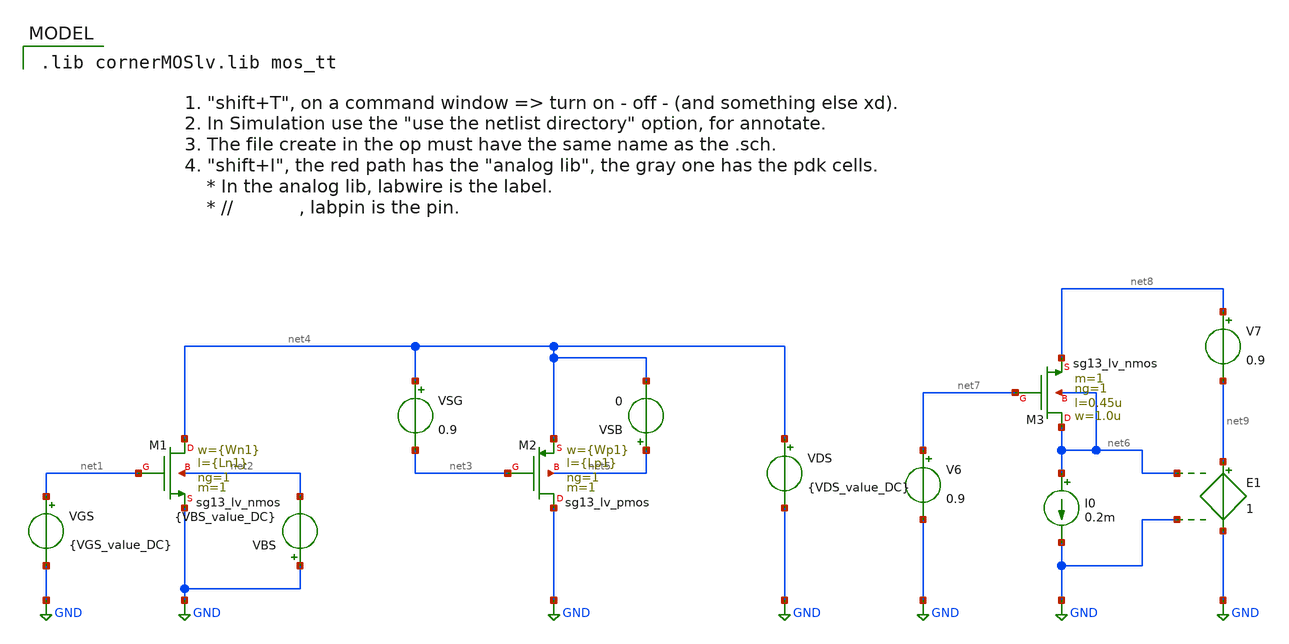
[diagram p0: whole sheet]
** sch_path: ADC8711-main/testbenches/tran/xschem/CMOSCHART_sg130_lv_tb.sch
**.subckt CMOSCHART_sg130_lv_tb
VGS net1 GND {VGS_value_DC}
VDS net4 GND {VDS_value_DC}
VBS GND net2 {VBS_value_DC}
VSG net4 net3 0.9
VSB net5 net4 0
I0 net6 GND 0.2m
V6 net7 GND 0.9
V7 net8 net9 0.9
E1 net9 GND net6 GND 1
XM1 net4 net1 GND net2 sg13_lv_nmos w={Wn1} l={Ln1} ng=1 m=1 mm_ok=1
XM2 GND net3 net4 net5 sg13_lv_pmos w={Wp1} l={Lp1} ng=1 m=1 mm_ok=1
XM3 net6 net7 net8 net6 sg13_lv_nmos w=1.0u l=0.45u ng=1 m=1 mm_ok=1
**** begin user architecture code



.op
.save all
.control

run
let Vgsn = @n.xm1.nsg13_lv_nmos[vgs]
let Vdsn = @n.xm1.nsg13_lv_nmos[vds]
let idn = @n.xm1.nsg13_lv_nmos[ids]
let gmn = @n.xm1.nsg13_lv_nmos[gm]
let vdsatn = @n.xm1.nsg13_lv_nmos[vsat]
let vthn = @n.xm1.nsg13_lv_nmos[vth]
let ron = @n.xm1.nsg13_lv_nmos[gds]
let cggn = @n.xm1.nsg13_lv_nmos[cgg]
let gm_idn = gmn/idn
let ftn = gmn / (6.283 * cggn)
let ftgm_idn = ftn * (gmn/idn)
let aon = gmn*ron
let Vovn = Vgsn - vthn
let deltaVdsn = Vdsn - vdsatn

print Vgsn Vdsn idn vdsatn vthn deltaVdsn Vovn gmn ron cggn gm_idn ftn ftgm_idn aon

write CMOSCHART_sg130_lv_tb.raw
set appendwrite


.endc





.save @n.xm1.nsg13_lv_nmos[ids]
.save @n.xm1.nsg13_lv_nmos[gm]
.save @n.xm1.nsg13_lv_nmos[vds]
.save @n.xm1.nsg13_lv_nmos[vsat]
.save @n.xm1.nsg13_lv_nmos[cgg]
.save @n.xm1.nsg13_lv_nmos[gds]


.dc VGS 0.0 1.8 0.01
.control
run

let idn = @n.xm1.nsg13_lv_nmos[ids]
let gmn = @n.xm1.nsg13_lv_nmos[gm]
let vdsatn = @n.xm1.nsg13_lv_nmos[vsat]
let gm_idn = gmn/idn
let cggn = @n.xm1.nsg13_lv_nmos[cgg]
let ftn = gmn/(6.283*cggn)
let ftgmidn = ftn*gm_idn
let ron = 1/@n.xm1.nsg13_lv_nmos[gds]
let aon = gmn*ron
let vds = @n.xm1.nsg13_lv_nmos[vds]
print vds

*use if you want to design with the gmoverid curve
meas dc VGS_meas WHEN gm_idn=13.57
*measure parameters of interest
meas dc aon_meas FIND aon WHEN v-sweep=VGS_meas
meas dc ftn_meas FIND ftn WHEN v-sweep=VGS_meas
meas dc idn_meas FIND idn WHEN v-sweep=VGS_meas
meas dc gmn_meas FIND gmn WHEN v-sweep=VGS_meas
meas dc gm_idn_meas FIND gm_idn WHEN v-sweep=VGS_meas

*use if you want to design with the vdsat curve
* To obtain the xvalue
*meas dc VGS_meas WHEN vdsatn=200m
* To obtain the yvalue
*meas dc gmn_meas FIND gmn WHEN v-sweep=VGS_meas

*plot idn
*plot vdsatn
*plot gmn
plot gm_idn
*plot cggn
*plot ftn
*plot ftgmidn
*plot aon

.endc


 .lib cornerMOSlv.lib mos_tt



.temp 65
.param Wn1=1u
.param Ln1=0.3u
.param Wp1=1u
.param Lp1=0.3u
.param VGS_value_DC=0.7248
.param VDS_value_DC=0.9
.param VBS_value_DC=0



**** end user architecture code
**.ends
.GLOBAL GND
.end
